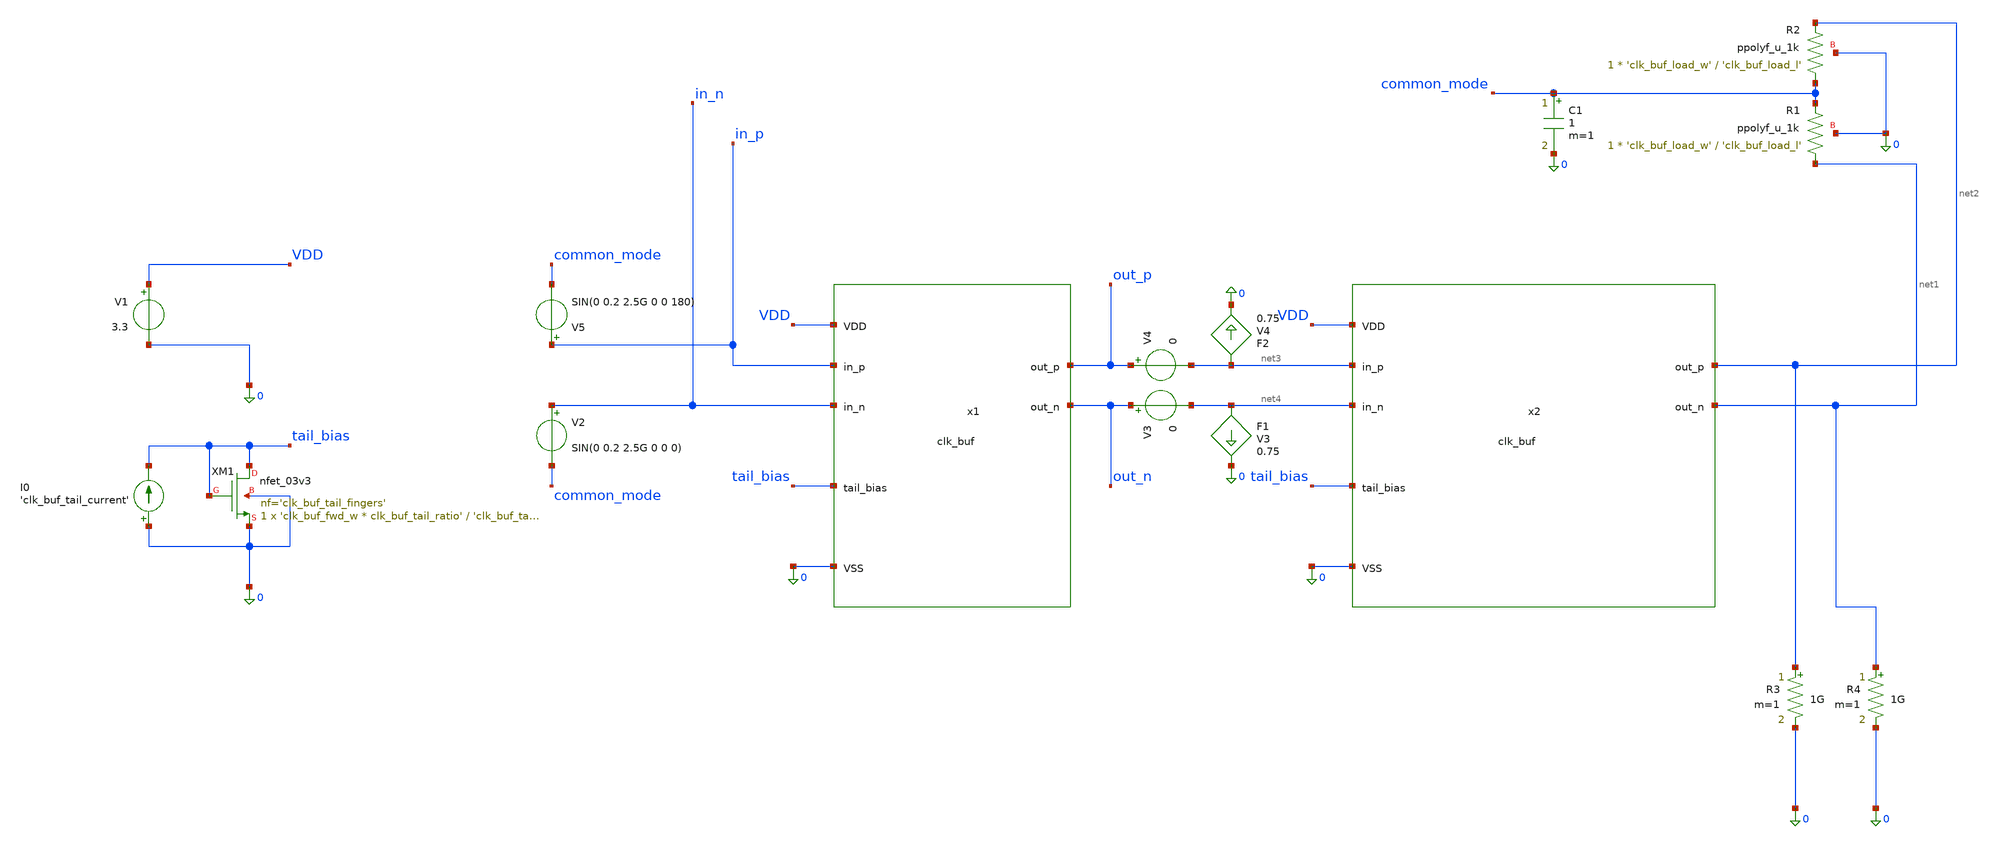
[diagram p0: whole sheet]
** sch_path: xschem/clk_buf_tb.sch
**.subckt clk_buf_tb
x1 0 VDD out_n out_p in_p in_n tail_bias clk_buf
XM1 tail_bias tail_bias 0 0 nfet_03v3 L='clk_buf_tail_l' W='clk_buf_fwd_w * clk_buf_tail_ratio' nf='clk_buf_tail_fingers'
+ ad='int((nf+1)/2) * W/nf * 0.18u' as='int((nf+2)/2) * W/nf * 0.18u' pd='2*int((nf+1)/2) * (W/nf + 0.18u)'
+ ps='2*int((nf+2)/2) * (W/nf + 0.18u)' nrd='0.18u / W' nrs='0.18u / W' sa=0 sb=0 sd=0 m=1
x2 0 VDD net1 net2 net3 net4 tail_bias clk_buf
V1 VDD 0 3.3
I0 0 tail_bias 'clk_buf_tail_current'
V2 in_n common_mode SIN(0 0.2 2.5G 0 0 0)
R3 net2 0 1G m=1
R4 net1 0 1G m=1
F1 net4 0 V3 0.75
XR1 net1 common_mode 0 ppolyf_u_1k r_width='clk_buf_load_w' r_length='clk_buf_load_l' m=1
F2 net3 0 V4 0.75
V3 out_n net4 0
V4 out_p net3 0
V5 in_p common_mode SIN(0 0.2 2.5G 0 0 180)
XR2 common_mode net2 0 ppolyf_u_1k r_width='clk_buf_load_w' r_length='clk_buf_load_l' m=1
C1 common_mode 0 1 m=1
**** begin user architecture code
 .include $::180MCU_MODELS/design.ngspice
.lib $::180MCU_MODELS/sm141064.ngspice typical
.lib $::180MCU_MODELS/sm141064.ngspice res_typical


.option savecurrents

.param clk_buf_fwd_w=6u
.param clk_buf_fwd_fingers=2
.param clk_buf_tail_fingers=20
.param clk_buf_tail_ratio=50
.param clk_buf_tail_l=1u
.param clk_buf_load_w=1u
.param clk_buf_load_r=4k
.param clk_buf_load_l='clk_buf_load_r/1000 * clk_buf_load_w'
.param clk_buf_tail_current=512u

.control
save all
tran 5p 5n
plot in_p in_n out_p out_n x1.net1
.endc
**** end user architecture code
**.ends

* expanding   symbol:  clk_buf.sym # of pins=7
** sym_path: xschem/clk_buf.sym
** sch_path: xschem/clk_buf.sch
.subckt clk_buf VSS VDD out_n out_p in_p in_n tail_bias
*.ipin VSS
*.ipin VDD
*.opin out_n
*.opin out_p
*.ipin in_p
*.ipin in_n
*.ipin tail_bias
XM1 out_n in_p net1 VSS nfet_03v3 L=0.28u W='clk_buf_fwd_w' nf='clk_buf_fwd_fingers' ad='int((nf+1)/2) * W/nf * 0.18u'
+ as='int((nf+2)/2) * W/nf * 0.18u' pd='2*int((nf+1)/2) * (W/nf + 0.18u)' ps='2*int((nf+2)/2) * (W/nf + 0.18u)'
+ nrd='0.18u / W' nrs='0.18u / W' sa=0 sb=0 sd=0 m=1
XM3 net1 tail_bias VSS VSS nfet_03v3 L='clk_buf_tail_l' W='clk_buf_fwd_w * clk_buf_tail_ratio' nf='clk_buf_tail_fingers'
+ ad='int((nf+1)/2) * W/nf * 0.18u' as='int((nf+2)/2) * W/nf * 0.18u' pd='2*int((nf+1)/2) * (W/nf + 0.18u)'
+ ps='2*int((nf+2)/2) * (W/nf + 0.18u)' nrd='0.18u / W' nrs='0.18u / W' sa=0 sb=0 sd=0 m=1
XM2 out_p in_n net1 VSS nfet_03v3 L=0.28u W='clk_buf_fwd_w' nf='clk_buf_fwd_fingers' ad='int((nf+1)/2) * W/nf * 0.18u'
+ as='int((nf+2)/2) * W/nf * 0.18u' pd='2*int((nf+1)/2) * (W/nf + 0.18u)' ps='2*int((nf+2)/2) * (W/nf + 0.18u)'
+ nrd='0.18u / W' nrs='0.18u / W' sa=0 sb=0 sd=0 m=1
XR1 out_n VDD VSS ppolyf_u_1k r_width='clk_buf_load_w' r_length='clk_buf_load_l' m=1
XR2 out_p VDD VSS ppolyf_u_1k r_width='clk_buf_load_w' r_length='clk_buf_load_l' m=1
.ends

.end
